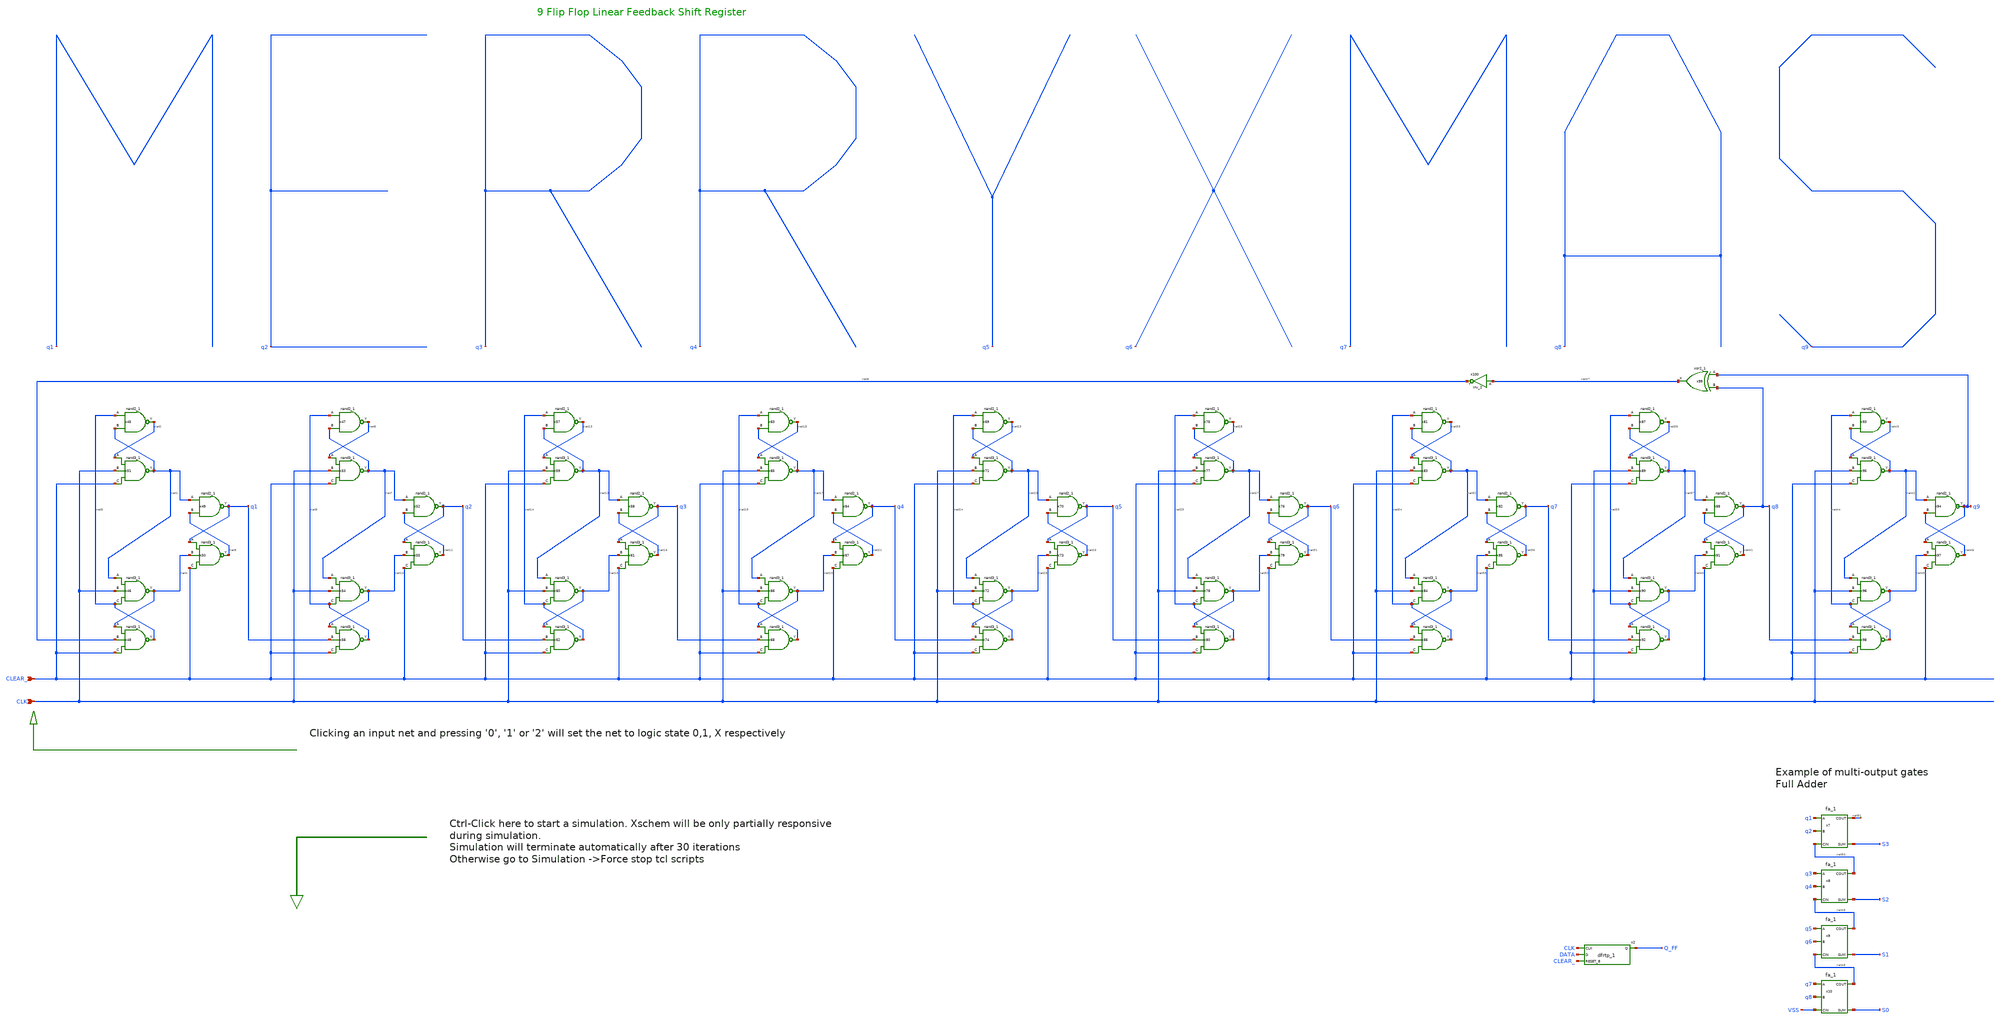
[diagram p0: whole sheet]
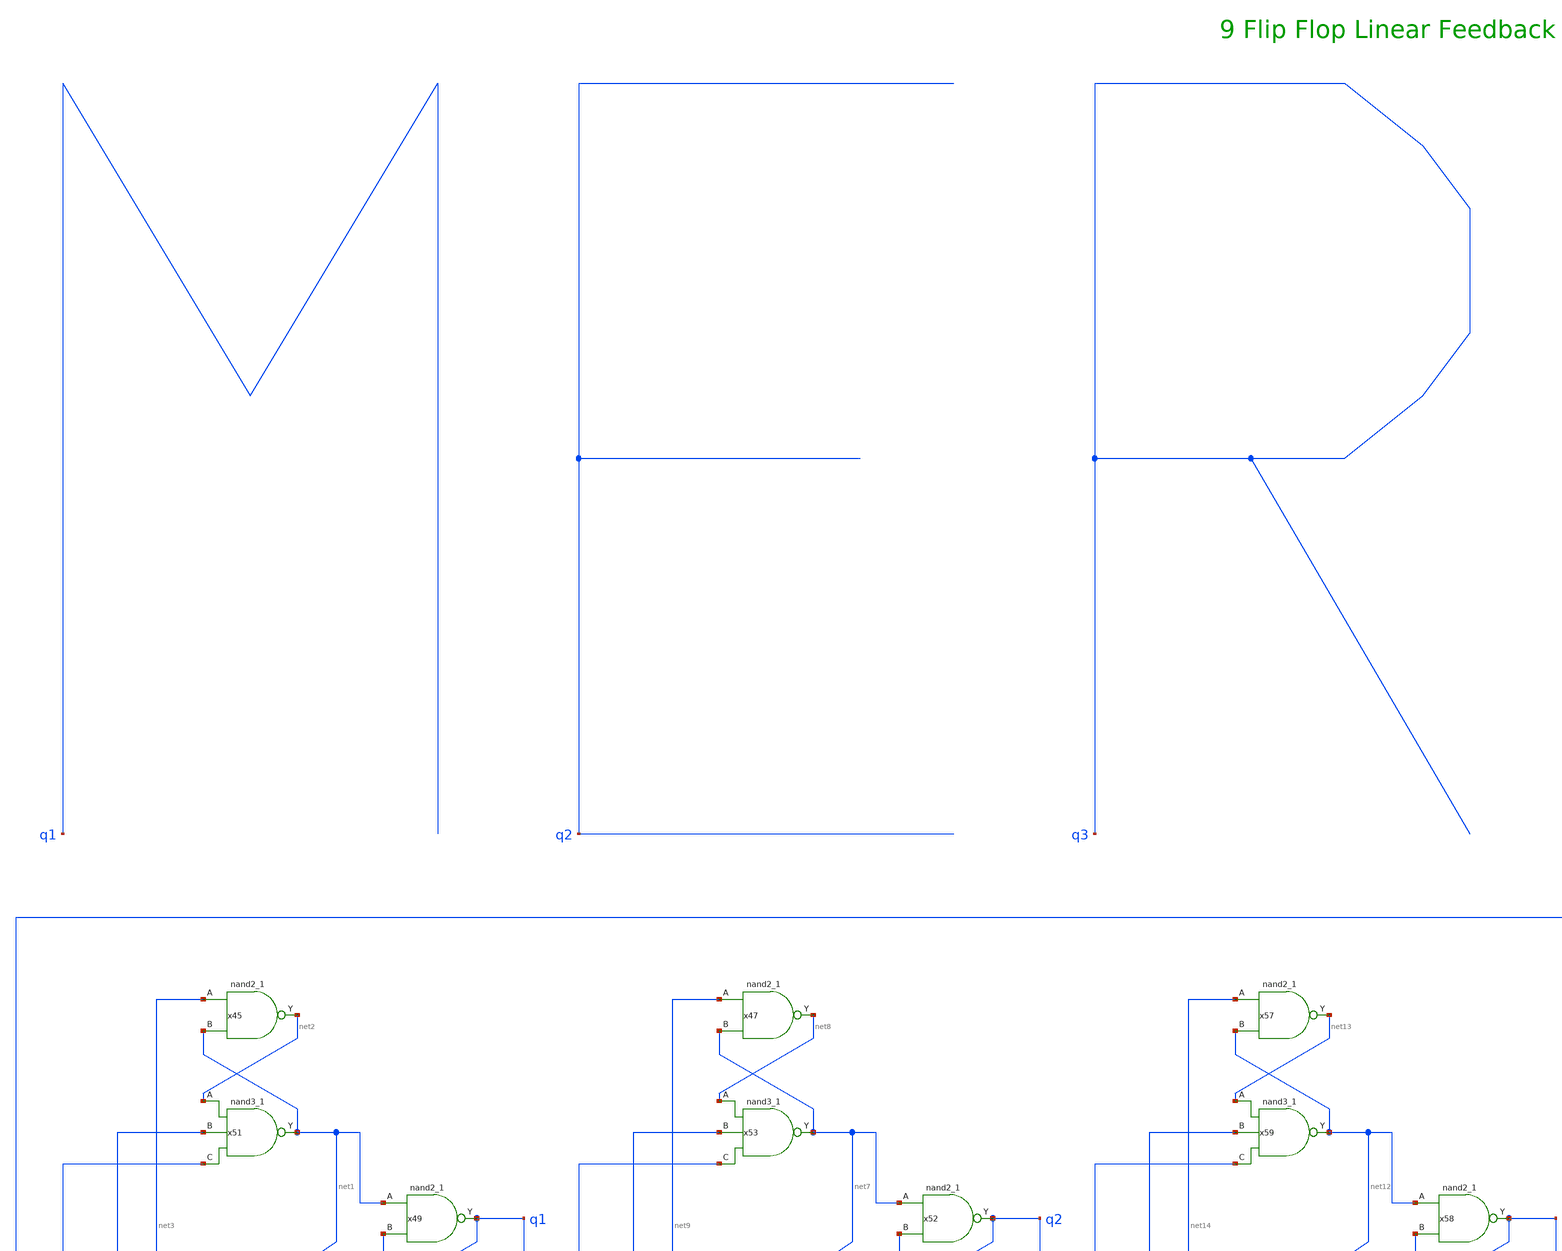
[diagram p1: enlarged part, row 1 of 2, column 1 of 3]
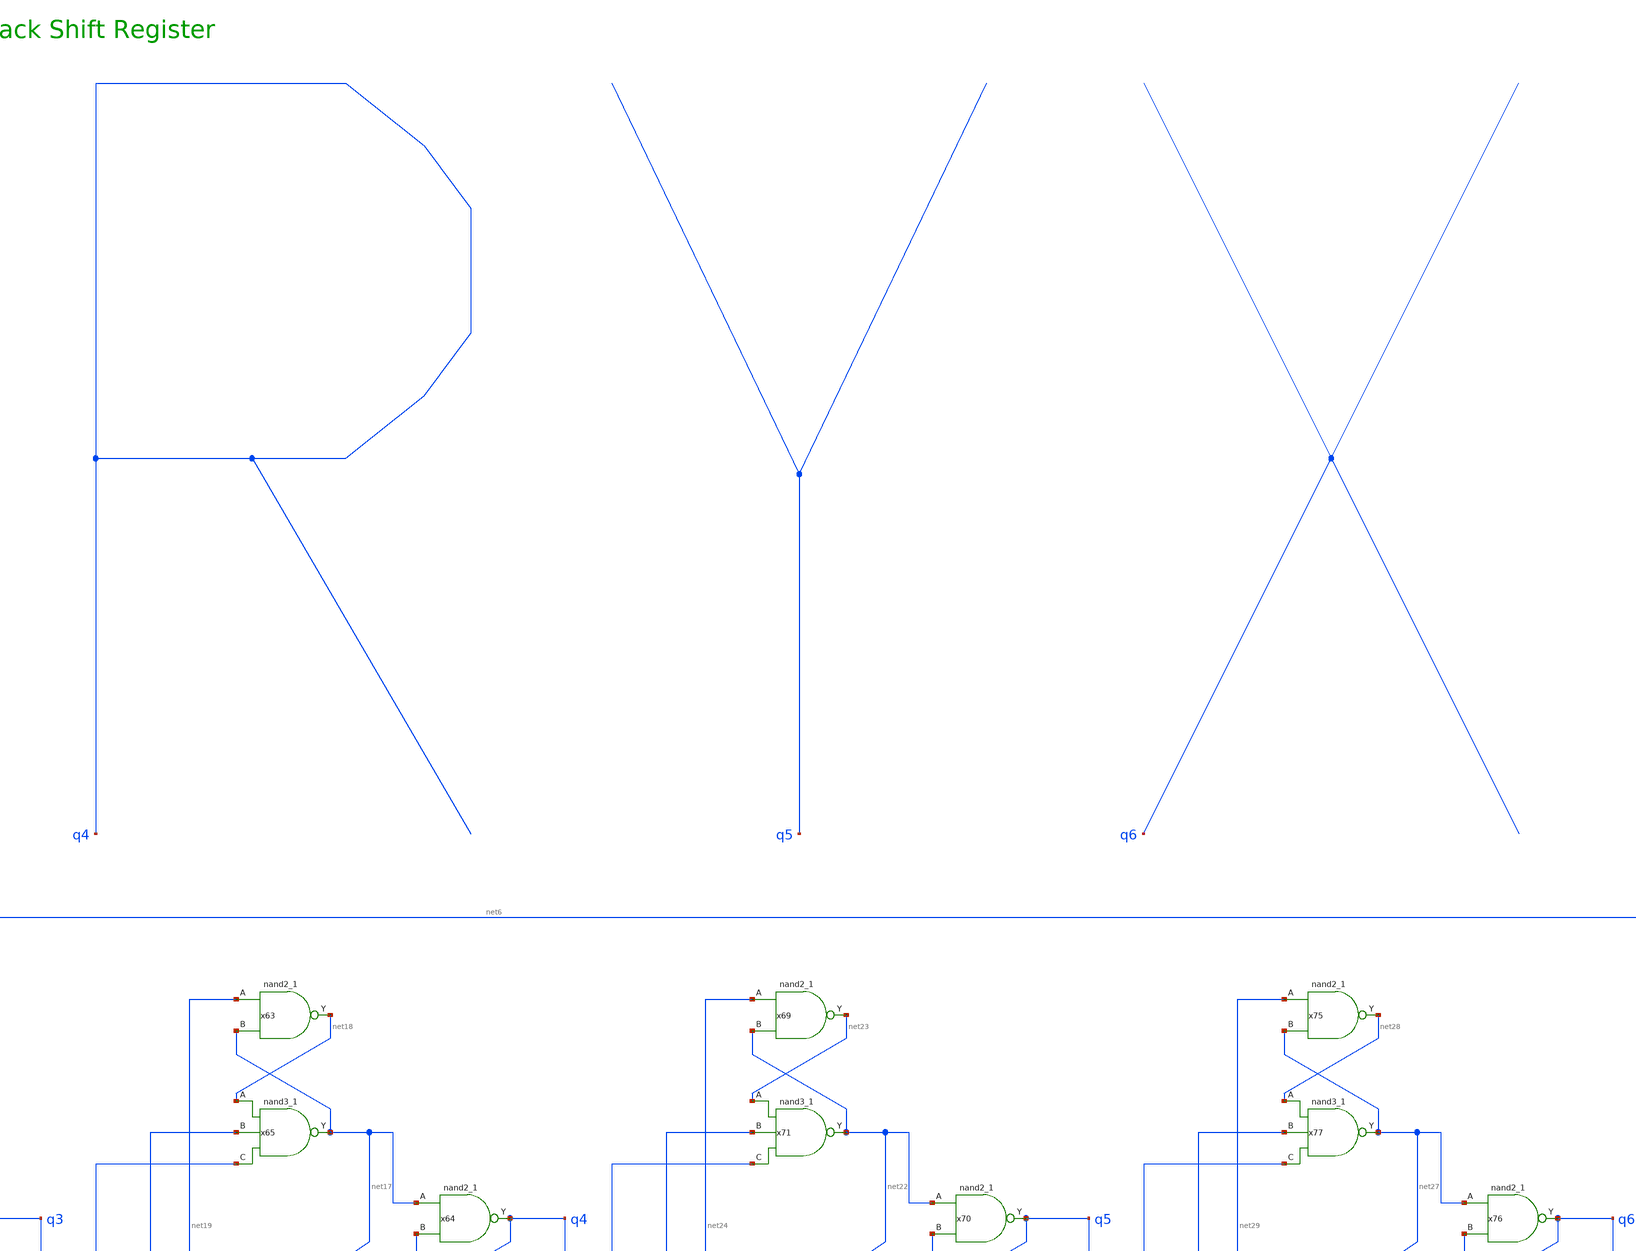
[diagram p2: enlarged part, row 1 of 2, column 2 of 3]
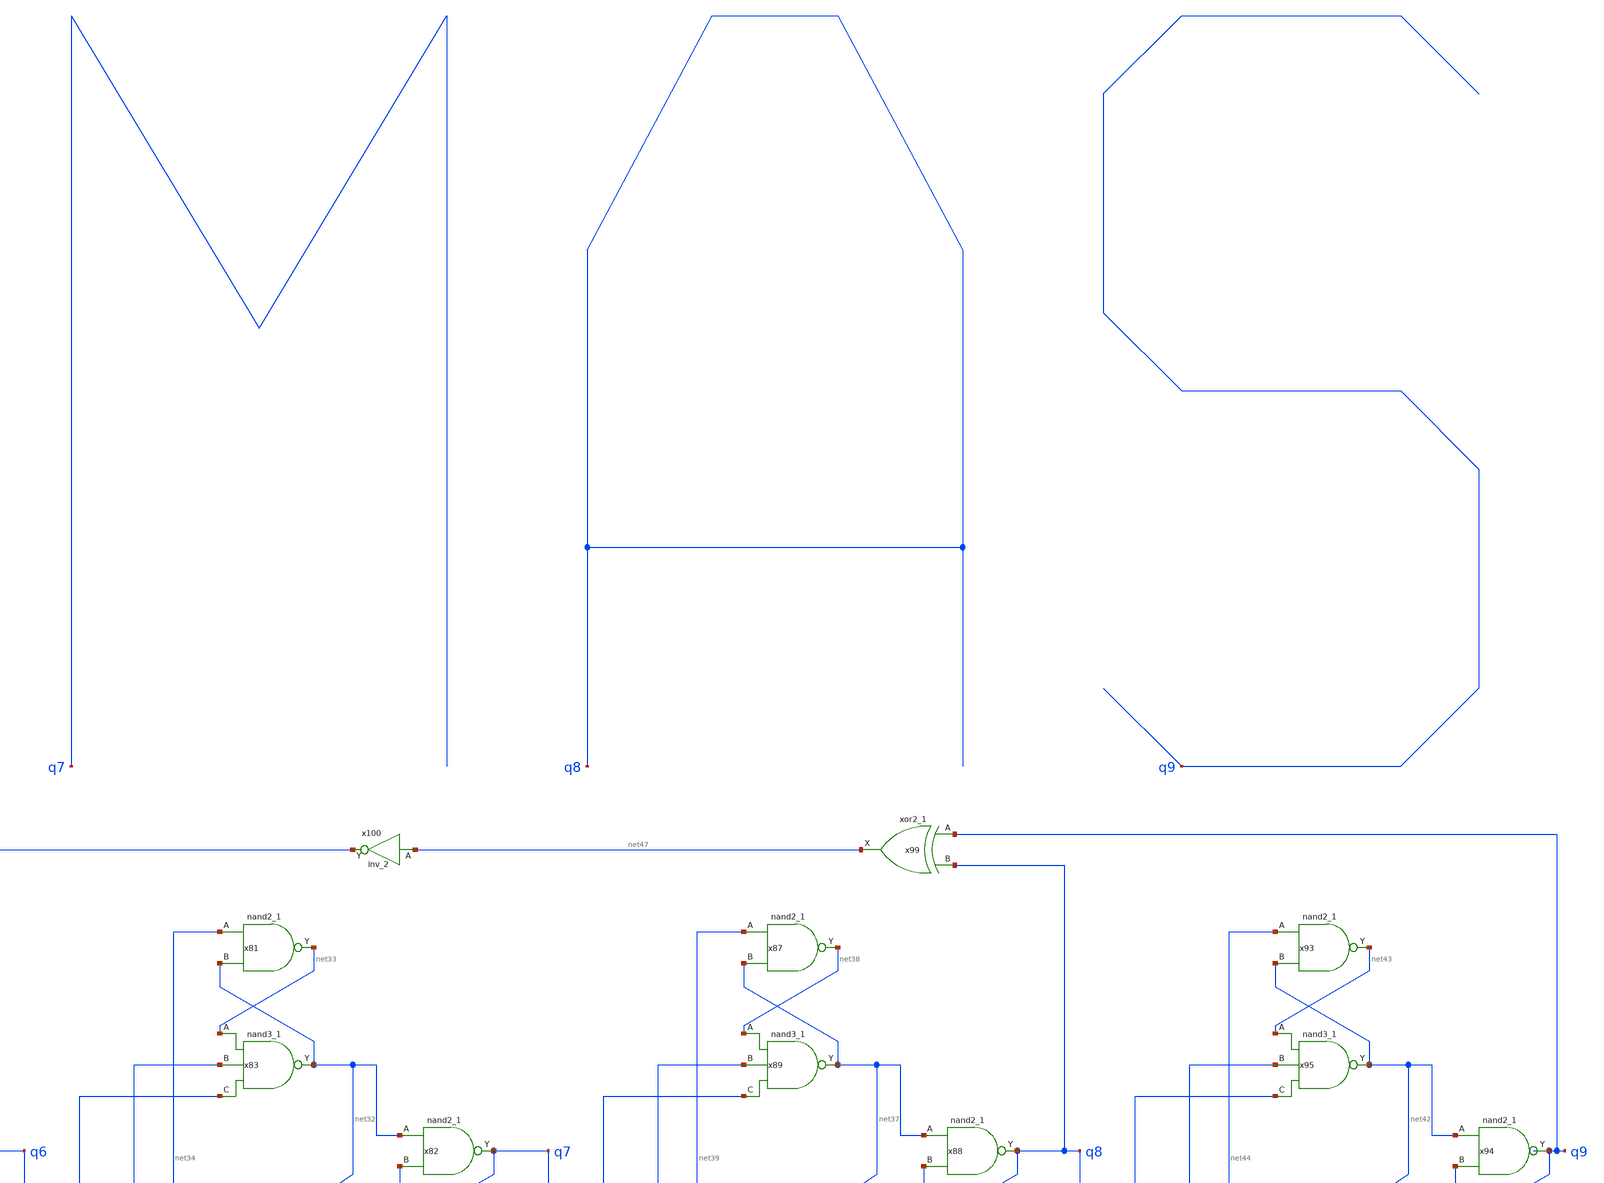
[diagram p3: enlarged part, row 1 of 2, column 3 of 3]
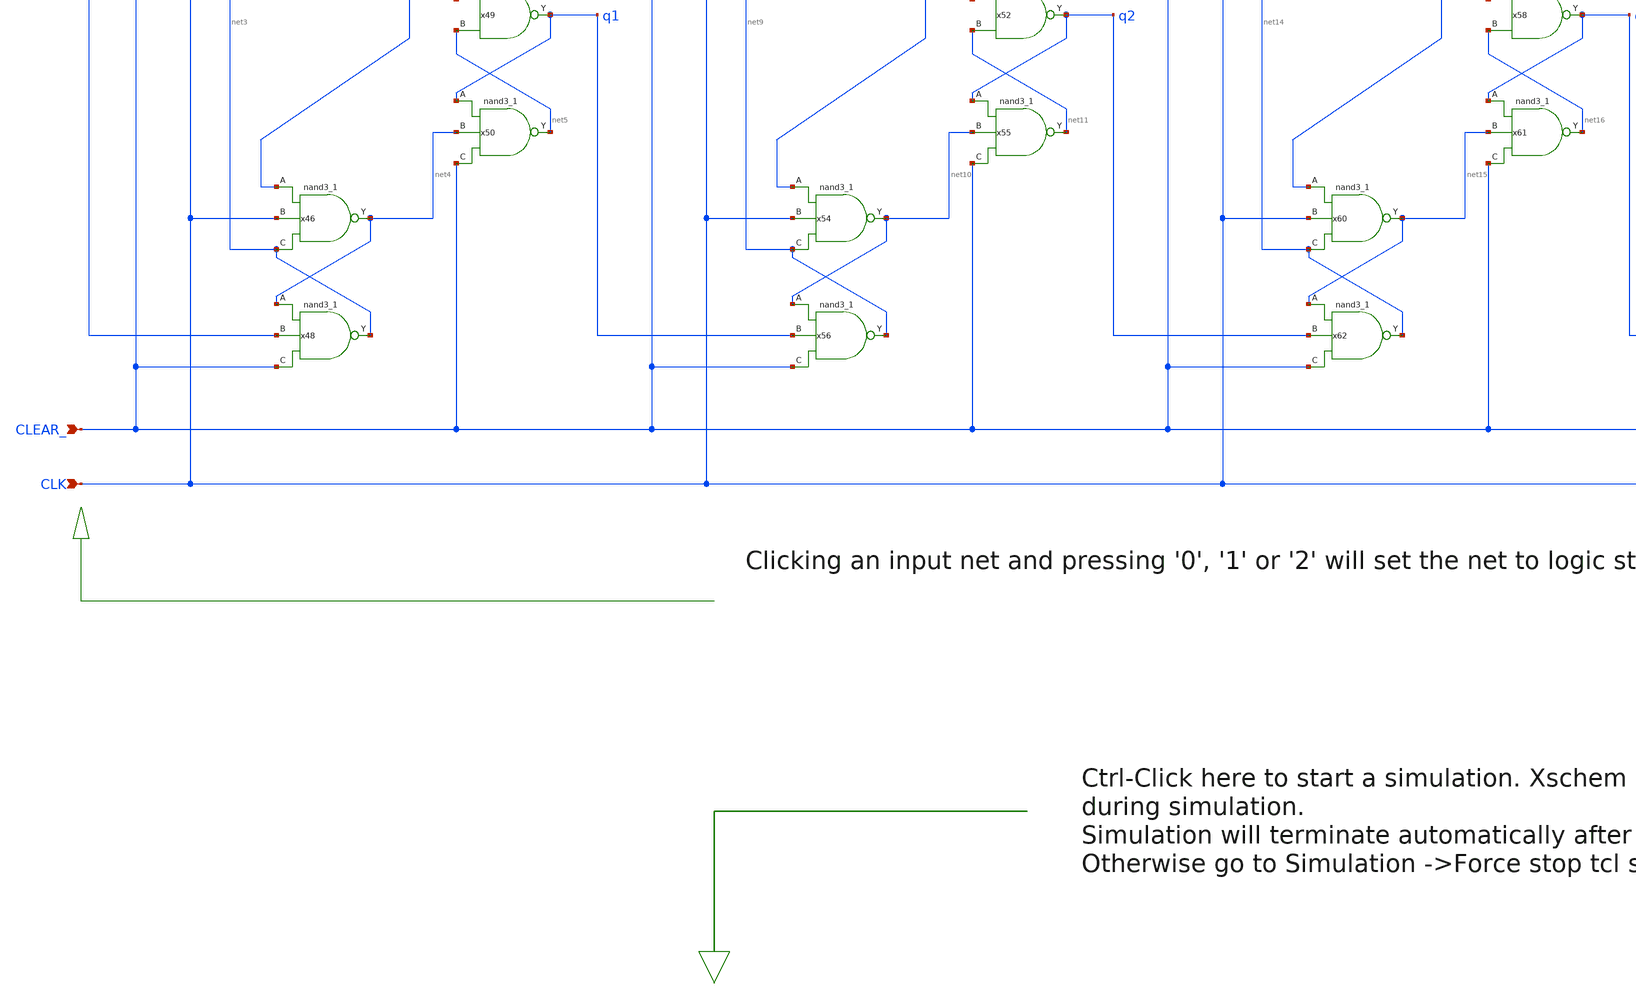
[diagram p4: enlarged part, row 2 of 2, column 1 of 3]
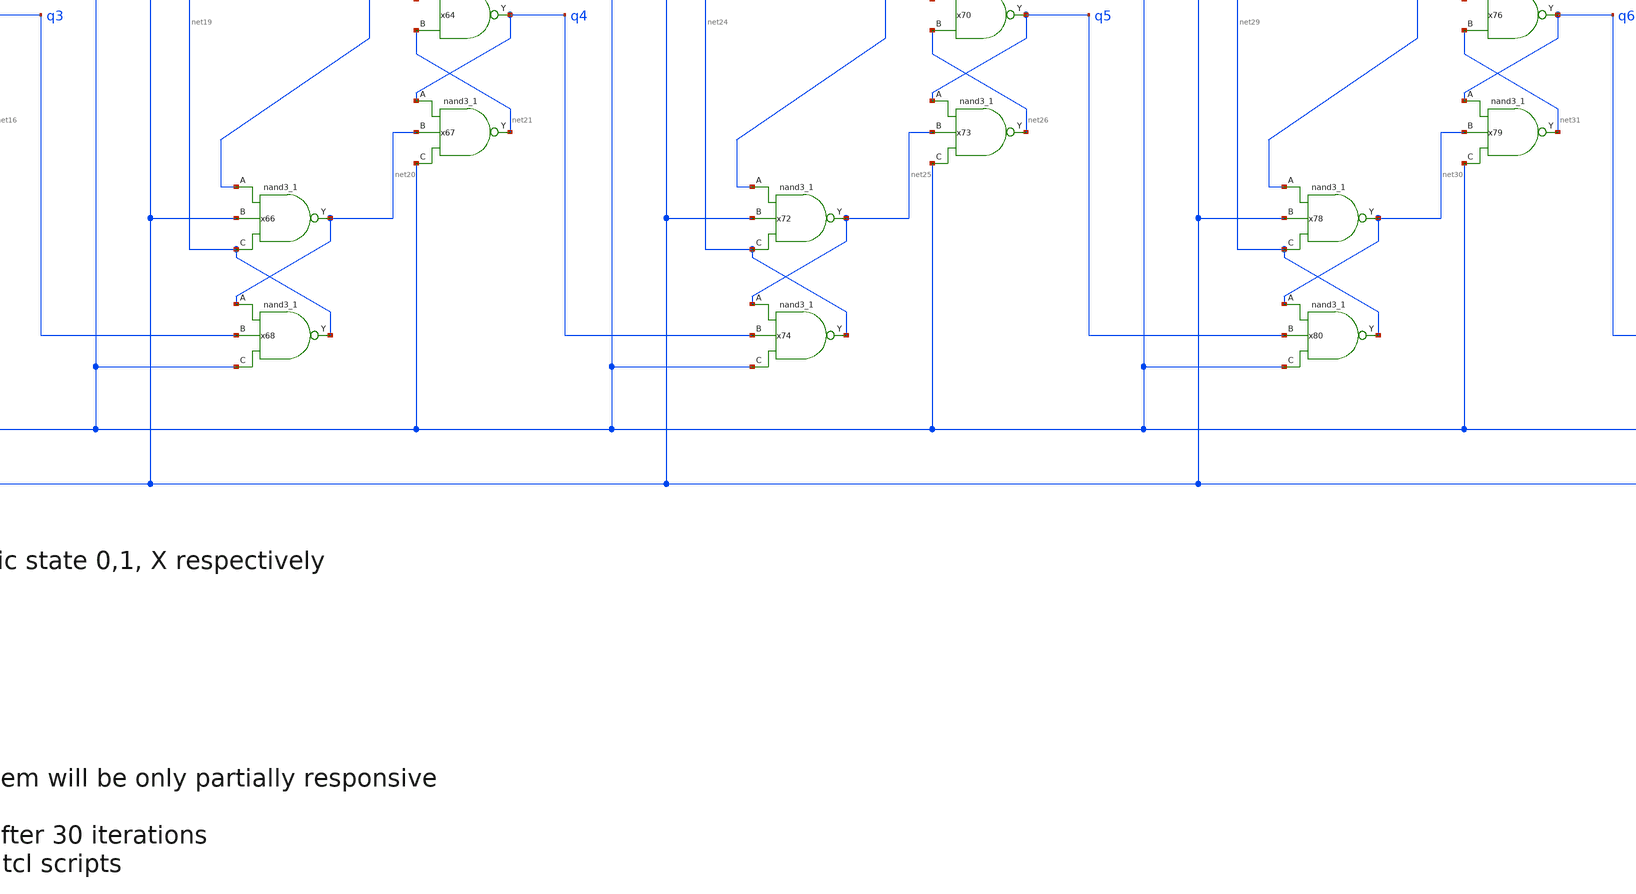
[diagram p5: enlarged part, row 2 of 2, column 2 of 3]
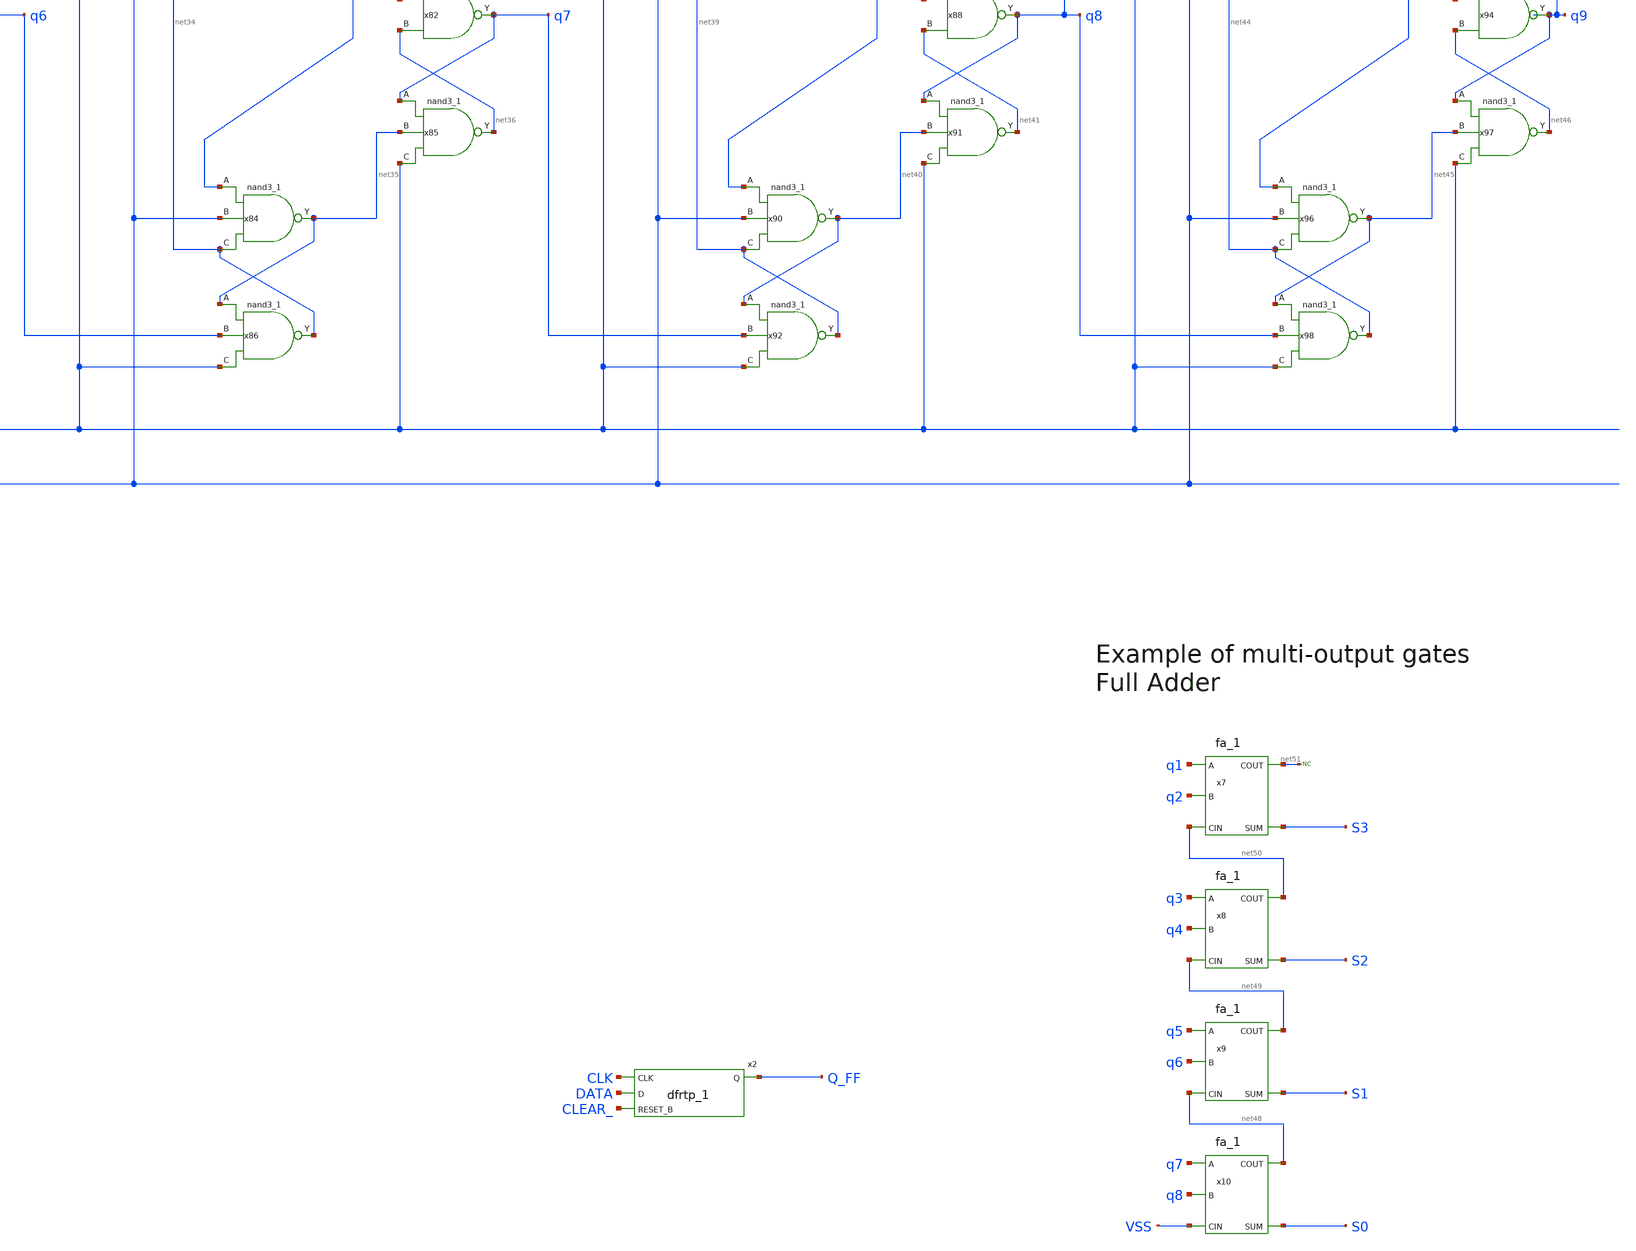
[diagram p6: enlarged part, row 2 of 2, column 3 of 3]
** sch_path: xschem_library/xschem_simulator/logic_test.sch
**.subckt logic_test CLK CLEAR_
*.ipin CLK
*.ipin CLEAR_
x45 net3 net1 VGND VNB VPB VPWR net2 sky130_fd_sc_hd__nand2_1
x49 net1 net5 VGND VNB VPB VPWR q1 sky130_fd_sc_hd__nand2_1
x51 net2 CLK CLEAR_ VGND VNB VPB VPWR net1 sky130_fd_sc_hd__nand3_1
x46 net1 CLK net3 VGND VNB VPB VPWR net4 sky130_fd_sc_hd__nand3_1
x50 q1 net4 CLEAR_ VGND VNB VPB VPWR net5 sky130_fd_sc_hd__nand3_1
x48 net4 net6 CLEAR_ VGND VNB VPB VPWR net3 sky130_fd_sc_hd__nand3_1
x47 net9 net7 VGND VNB VPB VPWR net8 sky130_fd_sc_hd__nand2_1
x52 net7 net11 VGND VNB VPB VPWR q2 sky130_fd_sc_hd__nand2_1
x53 net8 CLK CLEAR_ VGND VNB VPB VPWR net7 sky130_fd_sc_hd__nand3_1
x54 net7 CLK net9 VGND VNB VPB VPWR net10 sky130_fd_sc_hd__nand3_1
x55 q2 net10 CLEAR_ VGND VNB VPB VPWR net11 sky130_fd_sc_hd__nand3_1
x56 net10 q1 CLEAR_ VGND VNB VPB VPWR net9 sky130_fd_sc_hd__nand3_1
x57 net14 net12 VGND VNB VPB VPWR net13 sky130_fd_sc_hd__nand2_1
x58 net12 net16 VGND VNB VPB VPWR q3 sky130_fd_sc_hd__nand2_1
x59 net13 CLK CLEAR_ VGND VNB VPB VPWR net12 sky130_fd_sc_hd__nand3_1
x60 net12 CLK net14 VGND VNB VPB VPWR net15 sky130_fd_sc_hd__nand3_1
x61 q3 net15 CLEAR_ VGND VNB VPB VPWR net16 sky130_fd_sc_hd__nand3_1
x62 net15 q2 CLEAR_ VGND VNB VPB VPWR net14 sky130_fd_sc_hd__nand3_1
x63 net19 net17 VGND VNB VPB VPWR net18 sky130_fd_sc_hd__nand2_1
x64 net17 net21 VGND VNB VPB VPWR q4 sky130_fd_sc_hd__nand2_1
x65 net18 CLK CLEAR_ VGND VNB VPB VPWR net17 sky130_fd_sc_hd__nand3_1
x66 net17 CLK net19 VGND VNB VPB VPWR net20 sky130_fd_sc_hd__nand3_1
x67 q4 net20 CLEAR_ VGND VNB VPB VPWR net21 sky130_fd_sc_hd__nand3_1
x68 net20 q3 CLEAR_ VGND VNB VPB VPWR net19 sky130_fd_sc_hd__nand3_1
x69 net24 net22 VGND VNB VPB VPWR net23 sky130_fd_sc_hd__nand2_1
x70 net22 net26 VGND VNB VPB VPWR q5 sky130_fd_sc_hd__nand2_1
x71 net23 CLK CLEAR_ VGND VNB VPB VPWR net22 sky130_fd_sc_hd__nand3_1
x72 net22 CLK net24 VGND VNB VPB VPWR net25 sky130_fd_sc_hd__nand3_1
x73 q5 net25 CLEAR_ VGND VNB VPB VPWR net26 sky130_fd_sc_hd__nand3_1
x74 net25 q4 CLEAR_ VGND VNB VPB VPWR net24 sky130_fd_sc_hd__nand3_1
x75 net29 net27 VGND VNB VPB VPWR net28 sky130_fd_sc_hd__nand2_1
x76 net27 net31 VGND VNB VPB VPWR q6 sky130_fd_sc_hd__nand2_1
x77 net28 CLK CLEAR_ VGND VNB VPB VPWR net27 sky130_fd_sc_hd__nand3_1
x78 net27 CLK net29 VGND VNB VPB VPWR net30 sky130_fd_sc_hd__nand3_1
x79 q6 net30 CLEAR_ VGND VNB VPB VPWR net31 sky130_fd_sc_hd__nand3_1
x80 net30 q5 CLEAR_ VGND VNB VPB VPWR net29 sky130_fd_sc_hd__nand3_1
x81 net34 net32 VGND VNB VPB VPWR net33 sky130_fd_sc_hd__nand2_1
x82 net32 net36 VGND VNB VPB VPWR q7 sky130_fd_sc_hd__nand2_1
x83 net33 CLK CLEAR_ VGND VNB VPB VPWR net32 sky130_fd_sc_hd__nand3_1
x84 net32 CLK net34 VGND VNB VPB VPWR net35 sky130_fd_sc_hd__nand3_1
x85 q7 net35 CLEAR_ VGND VNB VPB VPWR net36 sky130_fd_sc_hd__nand3_1
x86 net35 q6 CLEAR_ VGND VNB VPB VPWR net34 sky130_fd_sc_hd__nand3_1
x87 net39 net37 VGND VNB VPB VPWR net38 sky130_fd_sc_hd__nand2_1
x88 net37 net41 VGND VNB VPB VPWR q8 sky130_fd_sc_hd__nand2_1
x89 net38 CLK CLEAR_ VGND VNB VPB VPWR net37 sky130_fd_sc_hd__nand3_1
x90 net37 CLK net39 VGND VNB VPB VPWR net40 sky130_fd_sc_hd__nand3_1
x91 q8 net40 CLEAR_ VGND VNB VPB VPWR net41 sky130_fd_sc_hd__nand3_1
x92 net40 q7 CLEAR_ VGND VNB VPB VPWR net39 sky130_fd_sc_hd__nand3_1
x93 net44 net42 VGND VNB VPB VPWR net43 sky130_fd_sc_hd__nand2_1
x94 net42 net46 VGND VNB VPB VPWR q9 sky130_fd_sc_hd__nand2_1
x95 net43 CLK CLEAR_ VGND VNB VPB VPWR net42 sky130_fd_sc_hd__nand3_1
x96 net42 CLK net44 VGND VNB VPB VPWR net45 sky130_fd_sc_hd__nand3_1
x97 q9 net45 CLEAR_ VGND VNB VPB VPWR net46 sky130_fd_sc_hd__nand3_1
x98 net45 q8 CLEAR_ VGND VNB VPB VPWR net44 sky130_fd_sc_hd__nand3_1
x99 q9 q8 VGND VNB VPB VPWR net47 sky130_fd_sc_hd__xor2_1
x100 net47 GND GND VCC VCC net6 sky130_fd_sc_hd__inv_1
x7 q1 q2 net50 VGND VNB VPB VPWR net51 S3 sky130_fd_sc_hd__fa_1
x8 q3 q4 net49 VGND VNB VPB VPWR net50 S2 sky130_fd_sc_hd__fa_1
x9 q5 q6 net48 VGND VNB VPB VPWR net49 S1 sky130_fd_sc_hd__fa_1
x10 q7 q8 VSS VGND VNB VPB VPWR net48 S0 sky130_fd_sc_hd__fa_1
* noconn #net51
x2 CLK DATA CLEAR_ VGND VNB VPB VPWR Q_FF sky130_fd_sc_hd__dfrtp_1
**.ends
.end
